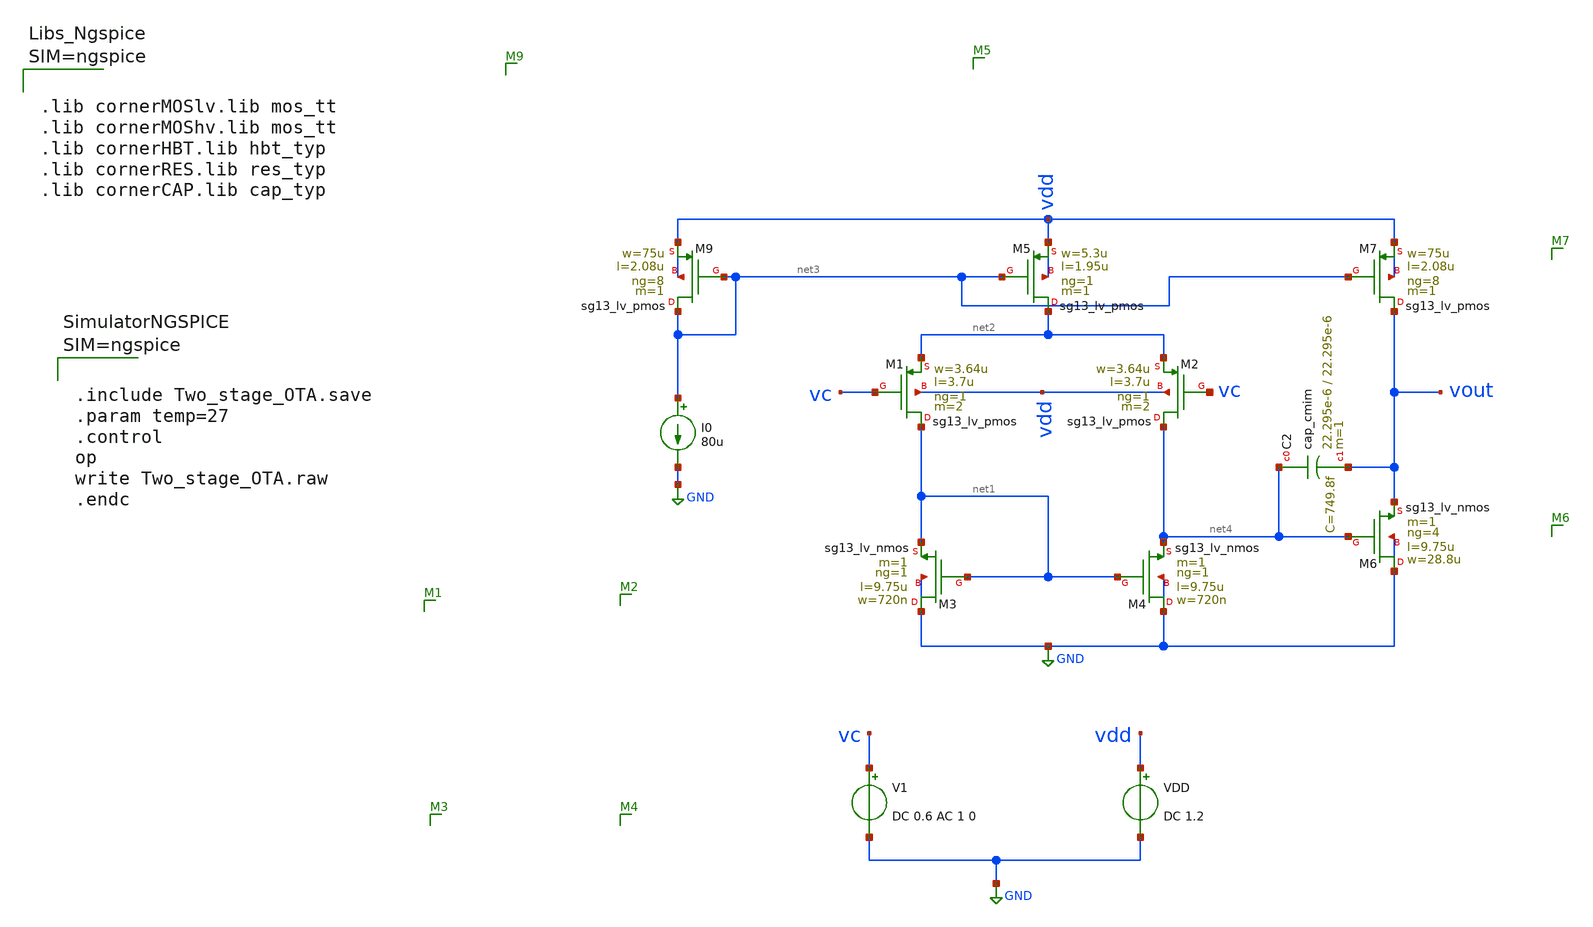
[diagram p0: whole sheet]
** sch_path: Schematics/lab_6/Two_stage_OTA.sch
**.subckt Two_stage_OTA
XM4 GND net1 net4 GND sg13_lv_nmos w=720n l=9.75u ng=1 m=1 mm_ok=1
XM3 GND net1 net1 GND sg13_lv_nmos w=720n l=9.75u ng=1 m=1 mm_ok=1
XM1 net1 vc net2 vdd sg13_lv_pmos w=3.64u l=3.7u ng=1 m=2 mm_ok=1
XM2 net4 vc net2 vdd sg13_lv_pmos w=3.64u l=3.7u ng=1 m=2 mm_ok=1
XM5 net2 net3 vdd vdd sg13_lv_pmos w=5.3u l=1.95u ng=1 m=1 mm_ok=1
XM7 vout net3 vdd vdd sg13_lv_pmos w=75u l=2.08u ng=8 m=1 mm_ok=1
XM6 GND net4 vout GND sg13_lv_nmos w=28.8u l=9.75u ng=4 m=1 mm_ok=1
XM9 net3 net3 vdd vdd sg13_lv_pmos w=75u l=2.08u ng=8 m=1 mm_ok=1
XC2 net4 vout cap_cmim w=22.295e-6 l=22.295e-6 m=1 mm_ok=1
I0 net3 GND 80u
V1 vc GND DC 0.6 AC 1 0
VDD vdd GND DC 1.2
**** begin user architecture code



.lib cornerMOSlv.lib mos_tt
.lib cornerMOShv.lib mos_tt
.lib cornerHBT.lib hbt_typ
.lib cornerRES.lib res_typ
.lib cornerCAP.lib cap_typ






.include Two_stage_OTA.save
.param temp=27
.control
op
write Two_stage_OTA.raw
.endc



**** end user architecture code
**.ends
.GLOBAL GND
.end
